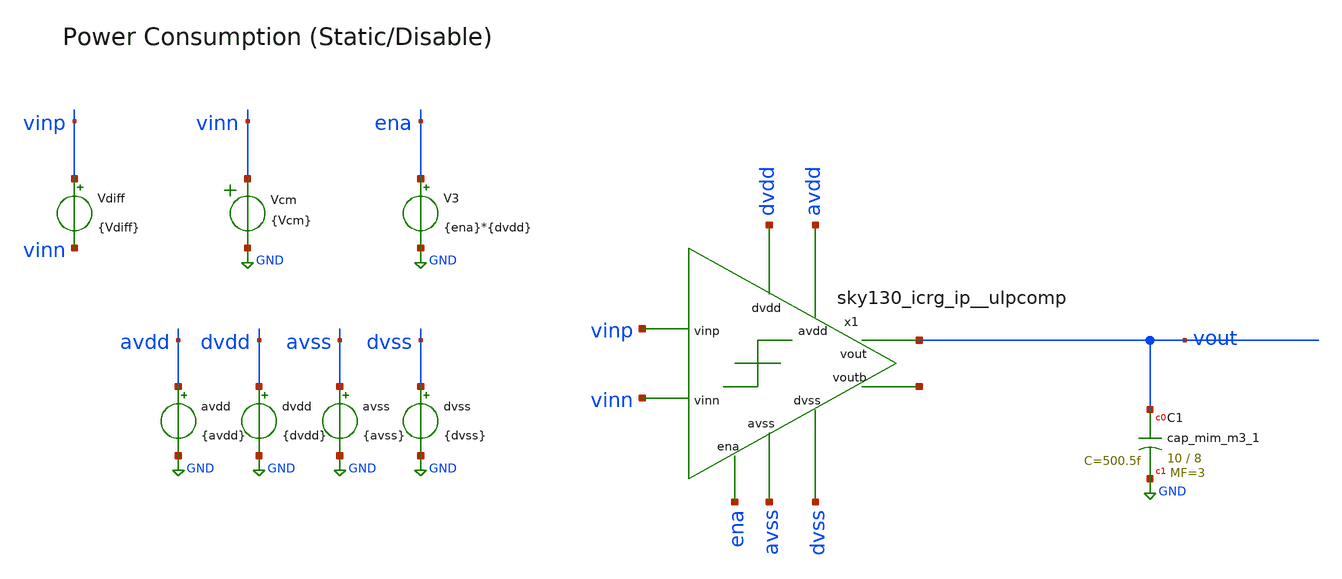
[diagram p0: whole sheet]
** sch_path: cace/tb_static_current.sch
**.subckt tb_static_current
V3 ena GND {ena}*{dvdd}
avdd avdd GND {avdd}
dvdd dvdd GND {dvdd}
avss avss GND {avss}
dvss dvss GND {dvss}
Vcm vinn GND VOL=' {Vcm} '
XC1 vout GND sky130_fd_pr__cap_mim_m3_1 W=10 L=8 MF=3 m=3
x1 dvdd avdd ena vinp vinn vout net1 avss dvss sky130_icrg_ip__ulpcomp
Vdiff vinp vinn {Vdiff}
**** begin user architecture code


.lib /home/ttuser/pdk/sky130A/libs.tech/combined/sky130.lib.spice {corner}
.option TEMP={temperature}


.control
op
set wr_singlescale
wrdata {simpath}/{filename}_{N}.data -I(dvdd)
quit
.endc

**** end user architecture code
**.ends
.GLOBAL GND
.end
